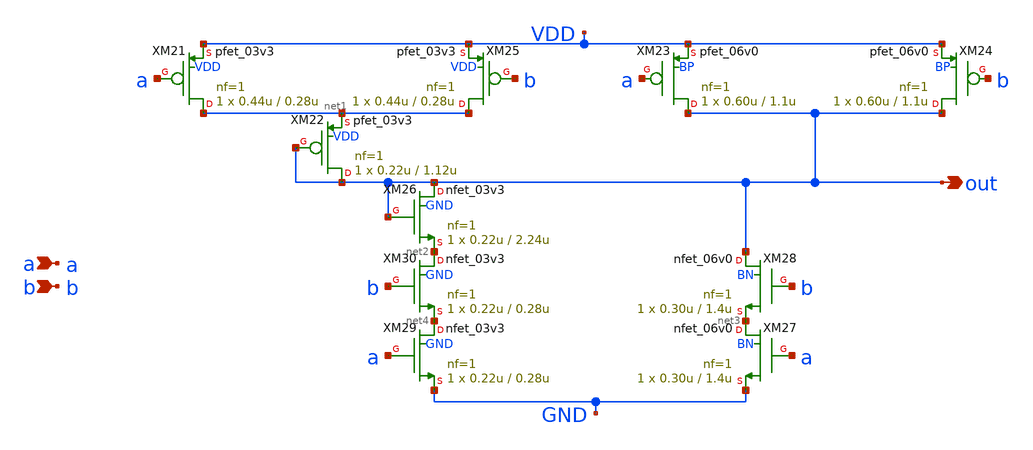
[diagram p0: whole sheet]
** sch_path: xschem_designs/NMIN.sch
**.subckt NMIN a b out
*.ipin a
*.ipin b
*.opin out
XM21 net1 a VDD VDD pfet_03v3 L=0.28u W=0.44u nf=1 ad='int((nf+1)/2) * W/nf * 0.18u' as='int((nf+2)/2) * W/nf * 0.18u'
+ pd='2*int((nf+1)/2) * (W/nf + 0.18u)' ps='2*int((nf+2)/2) * (W/nf + 0.18u)' nrd='0.18u / W' nrs='0.18u / W'
+ sa=0 sb=0 sd=0 m=1 par=1
XM22 out out net1 VDD pfet_03v3 L=1.12u W=0.22u nf=1 ad='int((nf+1)/2) * W/nf * 0.18u' as='int((nf+2)/2) * W/nf * 0.18u'
+ pd='2*int((nf+1)/2) * (W/nf + 0.18u)' ps='2*int((nf+2)/2) * (W/nf + 0.18u)' nrd='0.18u / W' nrs='0.18u / W'
+ sa=0 sb=0 sd=0 m=1 par=1
XM23 out a VDD BP pfet_06v0 L=1.1u W=0.60u nf=1 ad='int((nf+1)/2) * W/nf * 0.18u' as='int((nf+2)/2) * W/nf * 0.18u'
+ pd='2*int((nf+1)/2) * (W/nf + 0.18u)' ps='2*int((nf+2)/2) * (W/nf + 0.18u)' nrd='0.18u / W' nrs='0.18u / W'
+ sa=0 sb=0 sd=0 m=1 par=1
XM24 out b VDD BP pfet_06v0 L=1.1u W=0.60u nf=1 ad='int((nf+1)/2) * W/nf * 0.18u' as='int((nf+2)/2) * W/nf * 0.18u'
+ pd='2*int((nf+1)/2) * (W/nf + 0.18u)' ps='2*int((nf+2)/2) * (W/nf + 0.18u)' nrd='0.18u / W' nrs='0.18u / W'
+ sa=0 sb=0 sd=0 m=1 par=1
XM25 net1 b VDD VDD pfet_03v3 L=0.28u W=0.44u nf=1 ad='int((nf+1)/2) * W/nf * 0.18u' as='int((nf+2)/2) * W/nf * 0.18u'
+ pd='2*int((nf+1)/2) * (W/nf + 0.18u)' ps='2*int((nf+2)/2) * (W/nf + 0.18u)' nrd='0.18u / W' nrs='0.18u / W'
+ sa=0 sb=0 sd=0 m=1 par=1
XM26 out out net2 GND nfet_03v3 L=2.24u W=0.22u nf=1 ad='int((nf+1)/2) * W/nf * 0.18u' as='int((nf+2)/2) * W/nf * 0.18u'
+ pd='2*int((nf+1)/2) * (W/nf + 0.18u)' ps='2*int((nf+2)/2) * (W/nf + 0.18u)' nrd='0.18u / W' nrs='0.18u / W'
+ sa=0 sb=0 sd=0 m=1 par=1
XM27 net3 a GND BN nfet_06v0 L=1.4u W=0.30u nf=1 ad='int((nf+1)/2) * W/nf * 0.18u' as='int((nf+2)/2) * W/nf * 0.18u'
+ pd='2*int((nf+1)/2) * (W/nf + 0.18u)' ps='2*int((nf+2)/2) * (W/nf + 0.18u)' nrd='0.18u / W' nrs='0.18u / W'
+ sa=0 sb=0 sd=0 m=1 par=1
XM28 out b net3 BN nfet_06v0 L=1.4u W=0.30u nf=1 ad='int((nf+1)/2) * W/nf * 0.18u' as='int((nf+2)/2) * W/nf * 0.18u'
+ pd='2*int((nf+1)/2) * (W/nf + 0.18u)' ps='2*int((nf+2)/2) * (W/nf + 0.18u)' nrd='0.18u / W' nrs='0.18u / W'
+ sa=0 sb=0 sd=0 m=1 par=1
XM29 net4 a GND GND nfet_03v3 L=0.28u W=0.22u nf=1 ad='int((nf+1)/2) * W/nf * 0.18u' as='int((nf+2)/2) * W/nf * 0.18u'
+ pd='2*int((nf+1)/2) * (W/nf + 0.18u)' ps='2*int((nf+2)/2) * (W/nf + 0.18u)' nrd='0.18u / W' nrs='0.18u / W'
+ sa=0 sb=0 sd=0 m=1 par=1
XM30 net2 b net4 GND nfet_03v3 L=0.28u W=0.22u nf=1 ad='int((nf+1)/2) * W/nf * 0.18u' as='int((nf+2)/2) * W/nf * 0.18u'
+ pd='2*int((nf+1)/2) * (W/nf + 0.18u)' ps='2*int((nf+2)/2) * (W/nf + 0.18u)' nrd='0.18u / W' nrs='0.18u / W'
+ sa=0 sb=0 sd=0 m=1 par=1
**.ends
.end
